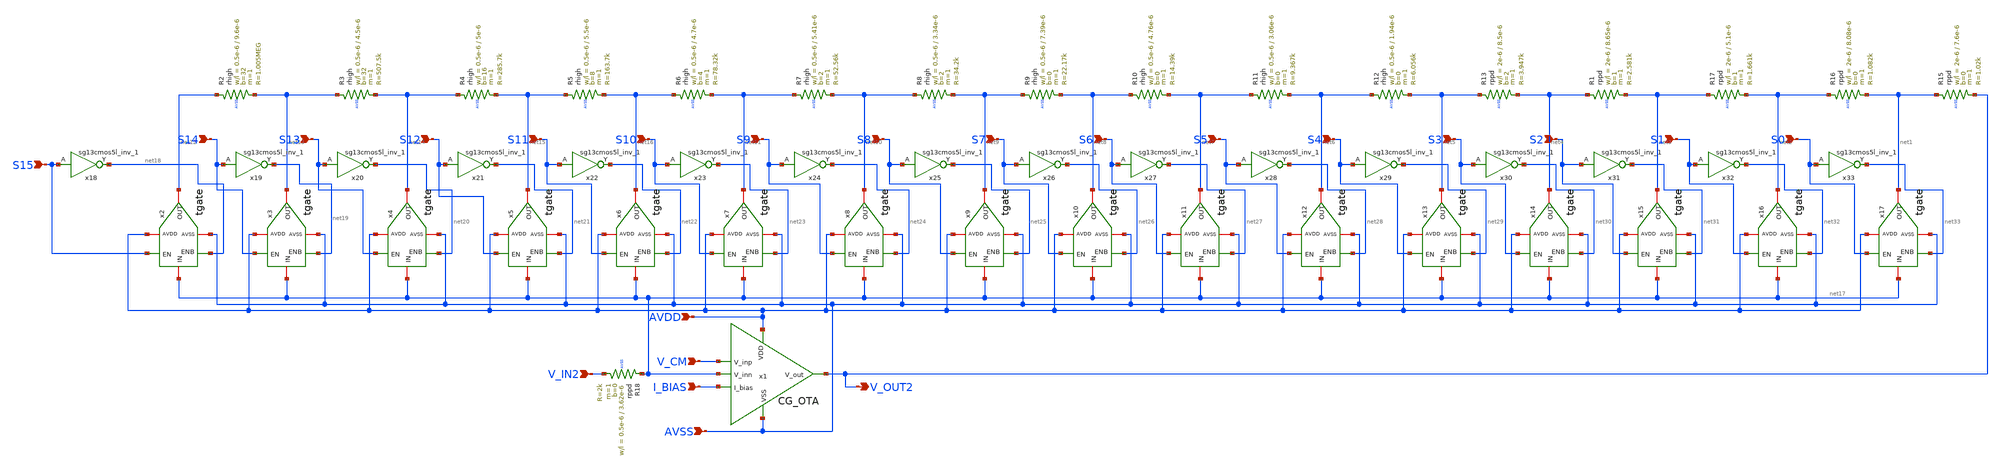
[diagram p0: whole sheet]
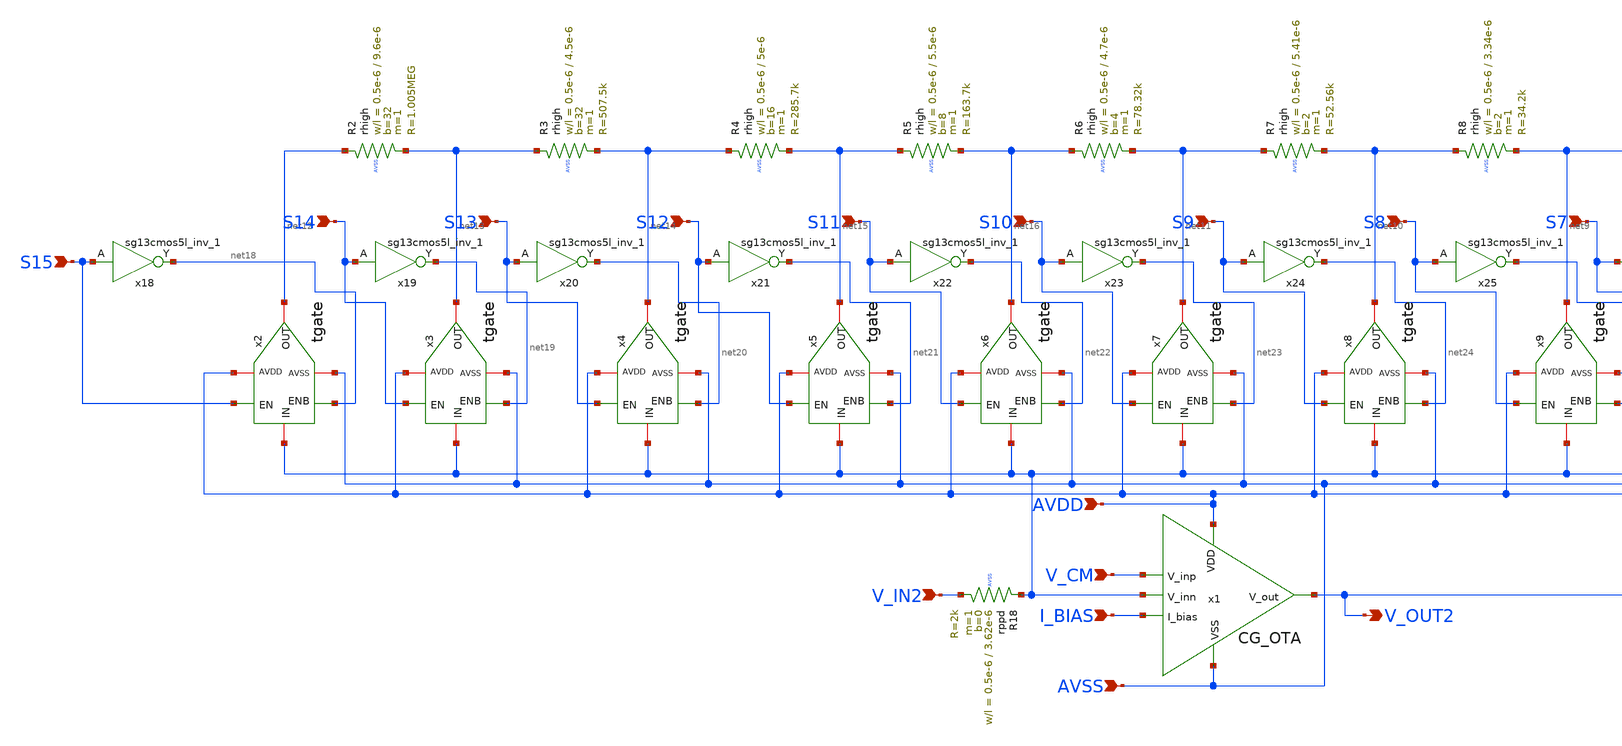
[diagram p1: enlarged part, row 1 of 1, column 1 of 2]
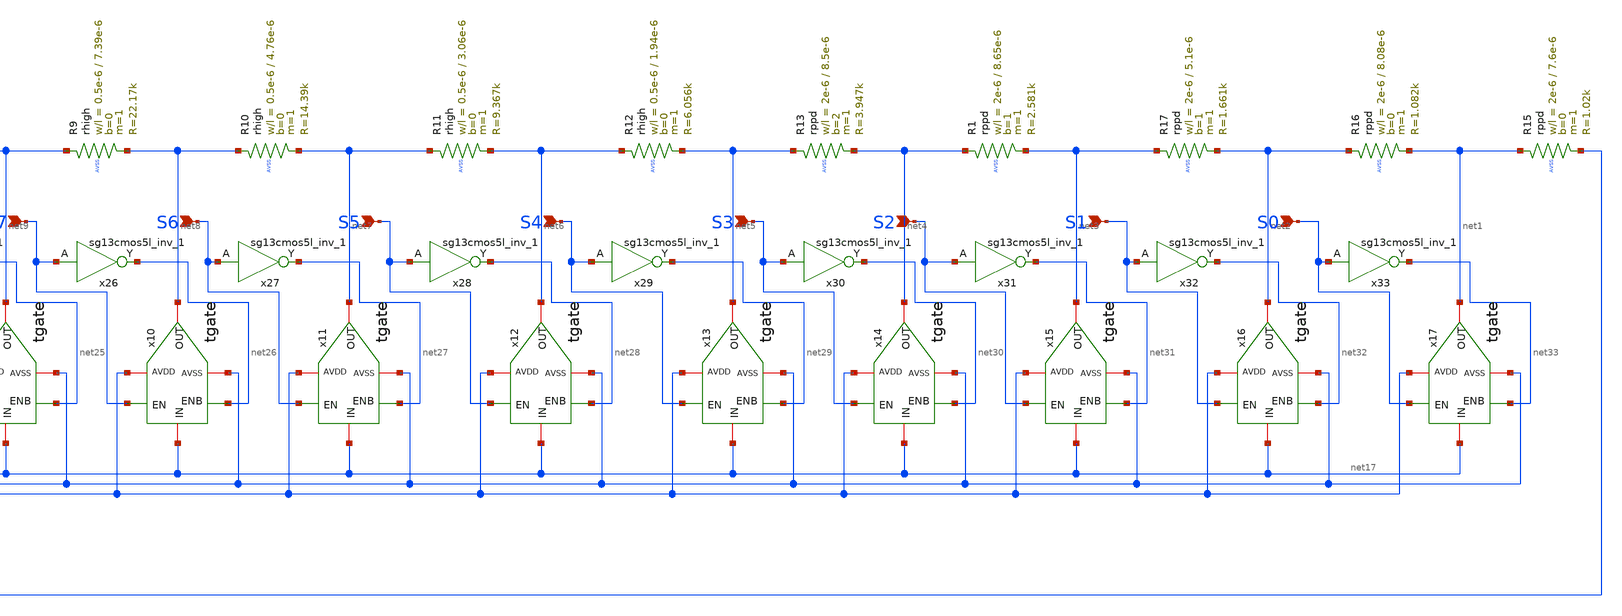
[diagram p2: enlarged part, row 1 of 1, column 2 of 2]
** sch_path: xschem/coarse_gain/cg_network.sch
**.subckt cg_network I_BIAS V_IN2 V_CM AVSS AVDD V_OUT2 S15 S14 S13 S12 S11 S10 S9 S8 S7 S6 S5 S4 S3
*+ S2 S1 S0
*.ipin I_BIAS
*.ipin V_IN2
*.ipin V_CM
*.ipin AVSS
*.ipin AVDD
*.opin V_OUT2
*.ipin S15
*.ipin S14
*.ipin S13
*.ipin S12
*.ipin S11
*.ipin S10
*.ipin S9
*.ipin S8
*.ipin S7
*.ipin S6
*.ipin S5
*.ipin S4
*.ipin S3
*.ipin S2
*.ipin S1
*.ipin S0
XR2 net12 net13 AVSS rhigh w=0.5e-6 l=9.6e-6 m=1 b=32 mm_ok=1
XR3 net13 net14 AVSS rhigh w=0.5e-6 l=4.5e-6 m=1 b=32 mm_ok=1
XR4 net14 net15 AVSS rhigh w=0.5e-6 l=5e-6 m=1 b=16 mm_ok=1
XR5 net15 net16 AVSS rhigh w=0.5e-6 l=5.5e-6 m=1 b=8 mm_ok=1
XR6 net16 net11 AVSS rhigh w=0.5e-6 l=4.7e-6 m=1 b=4 mm_ok=1
XR7 net11 net10 AVSS rhigh w=0.5e-6 l=5.41e-6 m=1 b=2 mm_ok=1
XR8 net10 net9 AVSS rhigh w=0.5e-6 l=3.34e-6 m=1 b=2 mm_ok=1
XR9 net9 net8 AVSS rhigh w=0.5e-6 l=7.39e-6 m=1 b=0 mm_ok=1
XR10 net8 net7 AVSS rhigh w=0.5e-6 l=4.76e-6 m=1 b=0 mm_ok=1
XR11 net7 net6 AVSS rhigh w=0.5e-6 l=3.06e-6 m=1 b=0 mm_ok=1
XR12 net6 net5 AVSS rhigh w=0.5e-6 l=1.94e-6 m=1 b=0 mm_ok=1
XR16 net2 net1 AVSS rppd w=2e-6 l=8.08e-6 m=1 b=0 mm_ok=1
XR17 net3 net2 AVSS rppd w=2e-6 l=5.1e-6 m=1 b=1 mm_ok=1
XR15 net1 V_OUT2 AVSS rppd w=2e-6 l=7.6e-6 m=1 b=0 mm_ok=1
XR18 net17 V_IN2 AVSS rppd w=0.5e-6 l=3.62e-6 m=1 b=0 mm_ok=1
XR1 net4 net3 AVSS rppd w=2e-6 l=8.65e-6 m=1 b=1 mm_ok=1
XR13 net5 net4 AVSS rppd w=2e-6 l=8.5e-6 m=1 b=2 mm_ok=1
x18 net18 S15 AVDD AVSS sg13cmos5l_inv_1
x19 net19 S14 AVDD AVSS sg13cmos5l_inv_1
x20 net20 S13 AVDD AVSS sg13cmos5l_inv_1
x21 net21 S12 AVDD AVSS sg13cmos5l_inv_1
x22 net22 S11 AVDD AVSS sg13cmos5l_inv_1
x23 net23 S10 AVDD AVSS sg13cmos5l_inv_1
x24 net24 S9 AVDD AVSS sg13cmos5l_inv_1
x25 net25 S8 AVDD AVSS sg13cmos5l_inv_1
x26 net26 S7 AVDD AVSS sg13cmos5l_inv_1
x27 net27 S6 AVDD AVSS sg13cmos5l_inv_1
x28 net28 S5 AVDD AVSS sg13cmos5l_inv_1
x29 net29 S4 AVDD AVSS sg13cmos5l_inv_1
x30 net30 S3 AVDD AVSS sg13cmos5l_inv_1
x31 net31 S2 AVDD AVSS sg13cmos5l_inv_1
x32 net32 S1 AVDD AVSS sg13cmos5l_inv_1
x33 net33 S0 AVDD AVSS sg13cmos5l_inv_1
x2 net17 AVSS AVDD S15 net18 net12 tgate l=0.13e-6 wn=0.15e-6 wp=0.45e-6
x3 net17 AVSS AVDD S14 net19 net13 tgate l=0.13e-6 wn=0.15e-6 wp=0.45e-6
x4 net17 AVSS AVDD S13 net20 net14 tgate l=0.13e-6 wn=0.15e-6 wp=0.45e-6
x5 net17 AVSS AVDD S12 net21 net15 tgate l=0.13e-6 wn=0.15e-6 wp=0.45e-6
x6 net17 AVSS AVDD S11 net22 net16 tgate l=0.13e-6 wn=0.15e-6 wp=0.45e-6
x7 net17 AVSS AVDD S10 net23 net11 tgate l=0.13e-6 wn=0.2e-6 wp=0.6e-6
x8 net17 AVSS AVDD S9 net24 net10 tgate l=0.13e-6 wn=0.5e-6 wp=1.5e-6
x9 net17 AVSS AVDD S8 net25 net9 tgate l=0.13e-6 wn=1e-6 wp=3e-6
x10 net17 AVSS AVDD S7 net26 net8 tgate l=0.13e-6 wn=1e-6 wp=3e-6
x11 net17 AVSS AVDD S6 net27 net7 tgate l=0.13e-6 wn=1.5e-6 wp=4.5e-6
x12 net17 AVSS AVDD S5 net28 net6 tgate l=0.13e-6 wn=2e-6 wp=6e-6
x13 net17 AVSS AVDD S4 net29 net5 tgate l=0.13e-6 wn=3e-6 wp=9e-6
x14 net17 AVSS AVDD S3 net30 net4 tgate l=0.13e-6 wn=3e-6 wp=9e-6
x15 net17 AVSS AVDD S2 net31 net3 tgate l=0.13e-6 wn=3e-6 wp=9e-6
x16 net17 AVSS AVDD S1 net32 net2 tgate l=0.13e-6 wn=3e-6 wp=9e-6
x17 net17 AVSS AVDD S0 net33 net1 tgate l=0.13e-6 wn=3e-6 wp=9e-6
x1 AVDD V_CM net17 V_OUT2 I_BIAS AVSS cg_ota
**.ends

* expanding   symbol:  /foss/designs/sg13cmos5l_spma_ip__instramp/xschem/tgate/tgate.sym # of pins=6
** sym_path: xschem/tgate/tgate.sym
** sch_path: xschem/tgate/tgate.sch
.subckt tgate IN AVSS AVDD EN ENB OUT  l=0.13e-6 wn=1e-6 wp=3e-6
*.iopin AVDD
*.iopin AVSS
*.iopin IN
*.iopin OUT
*.ipin EN
*.ipin ENB
XM1 IN EN OUT AVSS sg13_lv_nmos w=wn l=l ng=1 m=1 mm_ok=1
XM2 OUT ENB IN AVDD sg13_lv_pmos w=wp l=l ng=1 m=1 mm_ok=1
.ends


* expanding   symbol:  /foss/designs/sg13cmos5l_spma_ip__instramp/xschem/coarse_gain/cg_ota.sym # of
*+ pins=6
** sym_path: designs/libs/core_analog/coarse_gain/cg_ota.sym
** sch_path: designs/libs/core_analog/coarse_gain/cg_ota.sch
.subckt cg_ota VDD V_inp V_inn V_out I_bias VSS
*.ipin V_inn
*.ipin VDD
*.ipin VSS
*.opin V_out
*.ipin I_bias
*.ipin V_inp
XM1 F1 V_inn net6 VDD sg13_lv_pmos w=26.56u l=2u ng=4 m=1 mm_ok=1
XM2 F2 V_inp net6 VDD sg13_lv_pmos w=26.56u l=2u ng=4 m=1 mm_ok=1
XM3 net5 net5 VDD VDD sg13_lv_pmos w=7.33u l=2u ng=1 m=1 mm_ok=1
XM4 N_A net5 VDD VDD sg13_lv_pmos w=7.33u l=2u ng=1 m=1 mm_ok=1
XM7 F1 V_bn2 VSS VSS sg13_lv_nmos w=9.21u l=2u ng=1 m=1 mm_ok=1
XM8 F2 V_bn2 VSS VSS sg13_lv_nmos w=9.21u l=2u ng=1 m=1 mm_ok=1
XM_tail net6 V_btail VDD VDD sg13_lv_pmos w=7.46u l=2u ng=1 m=8 mm_ok=1
XM_ctrlp N_B V_ctrlp N_A VDD sg13_lv_pmos w=2.20u l=0.50u ng=1 m=1 mm_ok=1
XM_outp V_out N_A VDD VDD sg13_lv_pmos w=22.20u l=0.5u ng=4 m=1 mm_ok=1
XM_ctrln N_A V_ctrln N_B VSS sg13_lv_nmos w=0.84u l=0.5u ng=1 m=1 mm_ok=1
XM_outn V_out N_B VSS VSS sg13_lv_nmos w=8.4u l=0.5u ng=1 m=1 mm_ok=1
XM5 net5 V_bn1 F1 VSS sg13_lv_nmos w=6.41u l=2u ng=1 m=1 mm_ok=1
XM6 N_A V_bn1 F2 VSS sg13_lv_nmos w=6.41u l=2u ng=1 m=1 mm_ok=1
XM_mp1 net1 net1 VDD VDD sg13_lv_pmos w=2.30u l=2u ng=1 m=1 mm_ok=1
XM_mn1 net1 I_bias VSS VSS sg13_lv_nmos w=0.87u l=2u ng=1 m=1 mm_ok=1
XM_refn I_bias I_bias VSS VSS sg13_lv_nmos w=0.87u l=2u ng=1 m=1 mm_ok=1
XM_mp2 V_bn1 net1 VDD VDD sg13_lv_pmos w=11.50u l=2u ng=2 m=1 mm_ok=1
XM_mp3 V_bn2 net1 VDD VDD sg13_lv_pmos w=23u l=2u ng=4 m=1 mm_ok=1
XM_bn1 V_bn1 V_bn1 net2 VSS sg13_lv_nmos w=1.60u l=2u ng=1 m=1 mm_ok=1
XM_bn2 V_bn2 V_bn2 VSS VSS sg13_lv_nmos w=9.21u l=2u ng=1 m=1 mm_ok=1
XM_mn2 V_btail I_bias VSS VSS sg13_lv_nmos w=6u l=2u ng=1 m=1 mm_ok=1
XM_rep_tail V_btail V_btail VDD VDD sg13_lv_pmos w=7.46u l=2u ng=1 m=8 mm_ok=1
XM_mn4 N_B I_bias VSS VSS sg13_lv_nmos w=3.48u l=2u ng=1 m=1 mm_ok=1
XC1 F2 V_out cap_cmomf w=26.48e-6 l=26.48e-6 mmin=1 mmax=4 subblock=0 rfmodel=0 subscale=1 m=1
+ mm_ok=1
XC2 N_A V_out cap_cmomf w=22.07e-6 l=22.07e-6 mmin=1 mmax=4 subblock=0 rfmodel=0 subscale=1 m=1
+ mm_ok=1
XR1 net2 VSS VSS rhigh w=0.5e-6 l=17e-6 m=1 b=0 mm_ok=1
XM_mp4 V_ctrln net1 VDD VDD sg13_lv_pmos w=4.60u l=2u ng=1 m=1 mm_ok=1
XM_rep_ctrln V_ctrln V_ctrln net3 VSS sg13_lv_nmos w=0.84u l=0.5u ng=1 m=1 mm_ok=1
XM_rep_outn net3 net3 VSS VSS sg13_lv_nmos w=2.10u l=0.5u ng=1 m=1 mm_ok=1
XM_mn3 V_ctrlp I_bias VSS VSS sg13_lv_nmos w=1.74u l=2u ng=1 m=1 mm_ok=1
XM_rep_outp net4 net4 VDD VDD sg13_lv_pmos w=5.55u l=0.5u ng=1 m=1 mm_ok=1
XM_rep_ctrlp V_ctrlp V_ctrlp net4 VDD sg13_lv_pmos w=2.20u l=0.50u ng=1 m=1 mm_ok=1
XM_mp5 N_A net1 VDD VDD sg13_lv_pmos w=9.2u l=2u ng=1 m=1 mm_ok=1
.ends

.end
